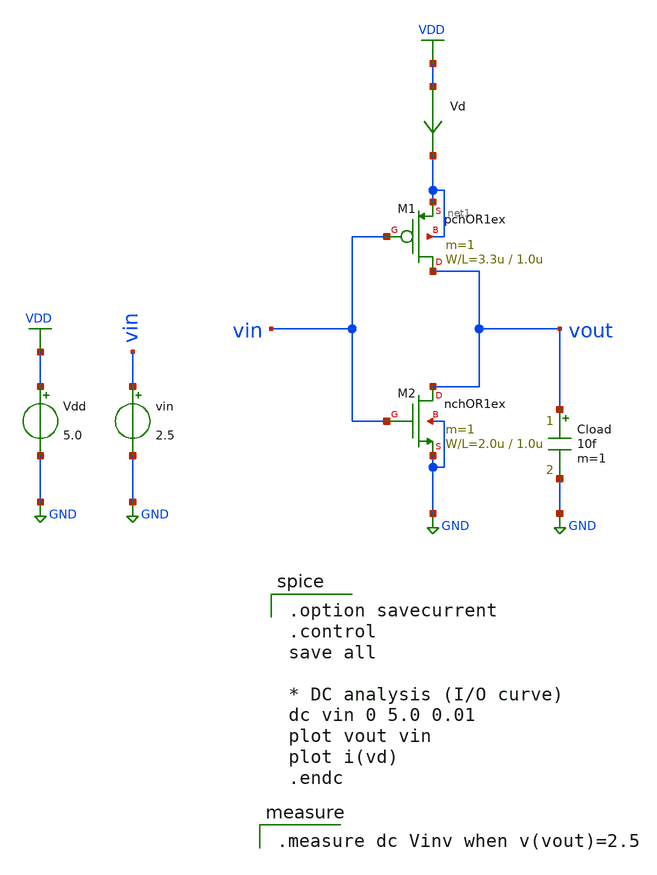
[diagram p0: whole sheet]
** sch_path: samples/inverter/PTS06/inverter_tb_mac.sch
**.subckt inverter_tb_mac
M2 vout vin GND GND nchOR1ex L=1.0u W=2.0u m=1
M1 vout vin net1 net1 pchOR1ex L=1.0u W=3.3u m=1
Vdd VDD GND 5.0
vin vin GND 2.5
Vd VDD net1 0
.save i(vd)
Cload vout GND 10f m=1
**** begin user architecture code
 .include /Users/[user]/.xschem/lib/PTS06/mos.lib
.include /Users/[user]/.xschem/lib/PTS06/stdcells.lib

.option savecurrent
.control
save all

* DC analysis (I/O curve)
dc vin 0 5.0 0.01
plot vout vin
plot i(vd)
.endc


.measure dc Vinv when v(vout)=2.5

**** end user architecture code
**.ends
.GLOBAL VDD
.GLOBAL GND
.end
